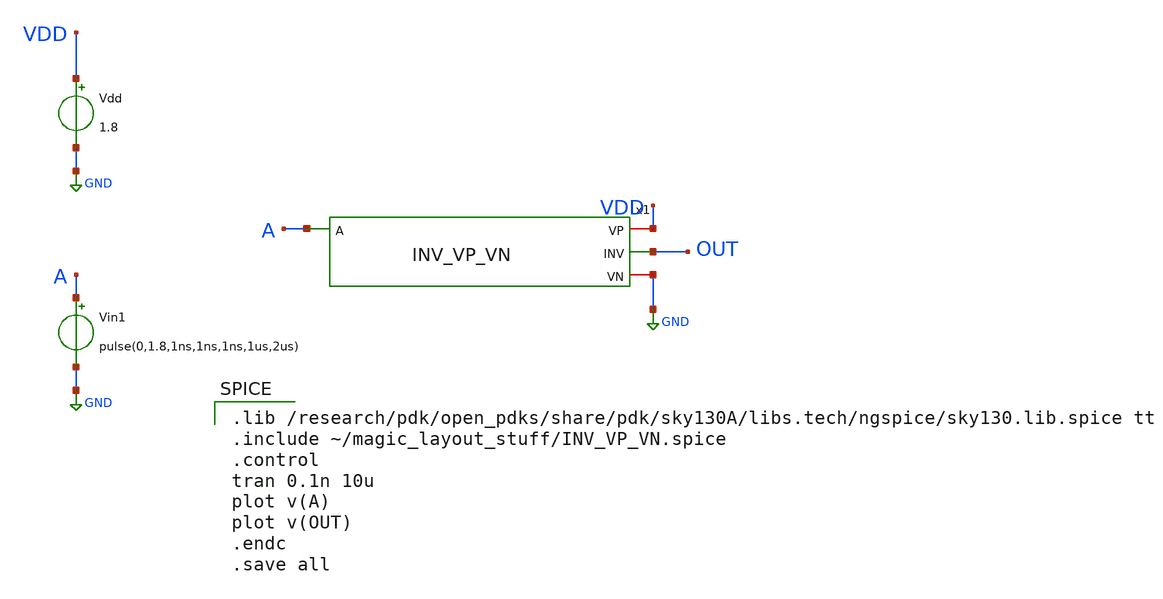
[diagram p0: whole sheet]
** sch_path: skywater_stuff/INV_VP_VN_sim.sch
**.subckt INV_VP_VN_sim
x1 VDD A OUT GND INV_VP_VN
Vdd VDD GND 1.8
Vin1 A GND pulse(0,1.8,1ns,1ns,1ns,1us,2us)
**** begin user architecture code

.lib /research/pdk/open_pdks/share/pdk/sky130A/libs.tech/ngspice/sky130.lib.spice tt
.include ~/magic_layout_stuff/INV_VP_VN.spice
.control
tran 0.1n 10u
plot v(A)
plot v(OUT)
.endc
.save all

**** end user architecture code
**.ends
.GLOBAL GND
.end
